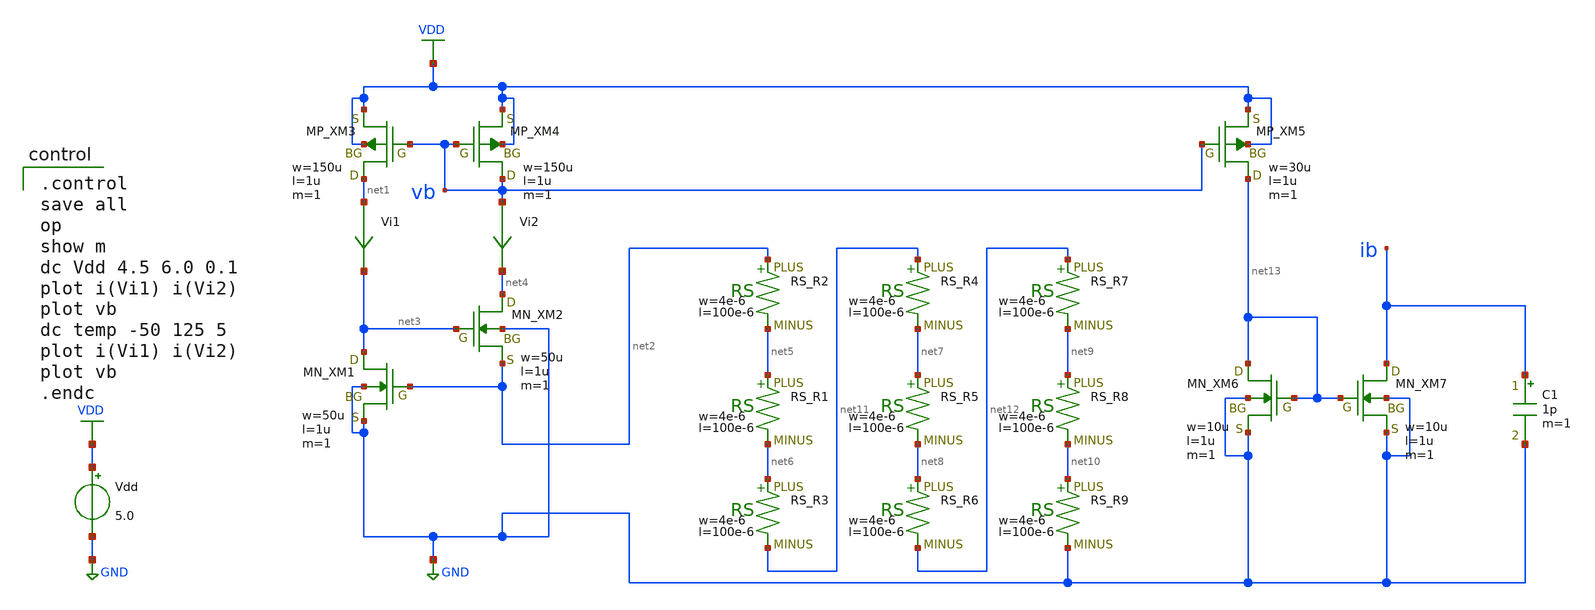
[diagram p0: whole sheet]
** sch_path: schematic/20250924_OSS_Workshop/ishikai/CS/cs-vth-ref_tb.sch
**.subckt cs-vth-ref_tb
Vdd VDD GND 5.0
Vi1 net1 net3 0
.save i(vi1)
Vi2 vb net4 0
.save i(vi2)
XM1 net3 net2 GND GND NMOS w=50u l=1u as=0 ad=0 ps=0 pd=0 nrd=0 nrs=0 m=1
XM2 net4 net3 net2 GND NMOS w=50u l=1u as=0 ad=0 ps=0 pd=0 nrd=0 nrs=0 m=1
XM3 net1 vb VDD VDD PMOS w=150u l=1u as=0 ad=0 ps=0 pd=0 nrd=0 nrs=0 m=1
XM4 vb vb VDD VDD PMOS w=150u l=1u as=0 ad=0 ps=0 pd=0 nrd=0 nrs=0 m=1
XR2 net2 net5 F_RS w=4e-6 R=2495 l=100e-6 tc1=0 tc2=0
XR1 net5 net6 F_RS w=4e-6 R=2495 l=100e-6 tc1=0 tc2=0
XR3 net6 net11 F_RS w=4e-6 R=2495 l=100e-6 tc1=0 tc2=0
XR4 net11 net7 F_RS w=4e-6 R=2495 l=100e-6 tc1=0 tc2=0
XR5 net7 net8 F_RS w=4e-6 R=2495 l=100e-6 tc1=0 tc2=0
XR6 net8 net12 F_RS w=4e-6 R=2495 l=100e-6 tc1=0 tc2=0
XR7 net12 net9 F_RS w=4e-6 R=2495 l=100e-6 tc1=0 tc2=0
XR8 net9 net10 F_RS w=4e-6 R=2495 l=100e-6 tc1=0 tc2=0
XR9 net10 GND F_RS w=4e-6 R=2495 l=100e-6 tc1=0 tc2=0
XM5 net13 vb VDD VDD PMOS w=30u l=1u as=0 ad=0 ps=0 pd=0 nrd=0 nrs=0 m=1
XM6 net13 net13 GND GND NMOS w=10u l=1u as=0 ad=0 ps=0 pd=0 nrd=0 nrs=0 m=1
XM7 ib net13 GND GND NMOS w=10u l=1u as=0 ad=0 ps=0 pd=0 nrd=0 nrs=0 m=1
C1 ib GND 1p m=1
**** begin user architecture code

.control
save all
op
show m
dc Vdd 4.5 6.0 0.1
plot i(Vi1) i(Vi2)
plot vb
dc temp -50 125 5
plot i(Vi1) i(Vi2)
plot vb
.endc

 .include $::LIB/../ip62_models
**** end user architecture code
**.ends
.GLOBAL GND
.GLOBAL VDD
.end
